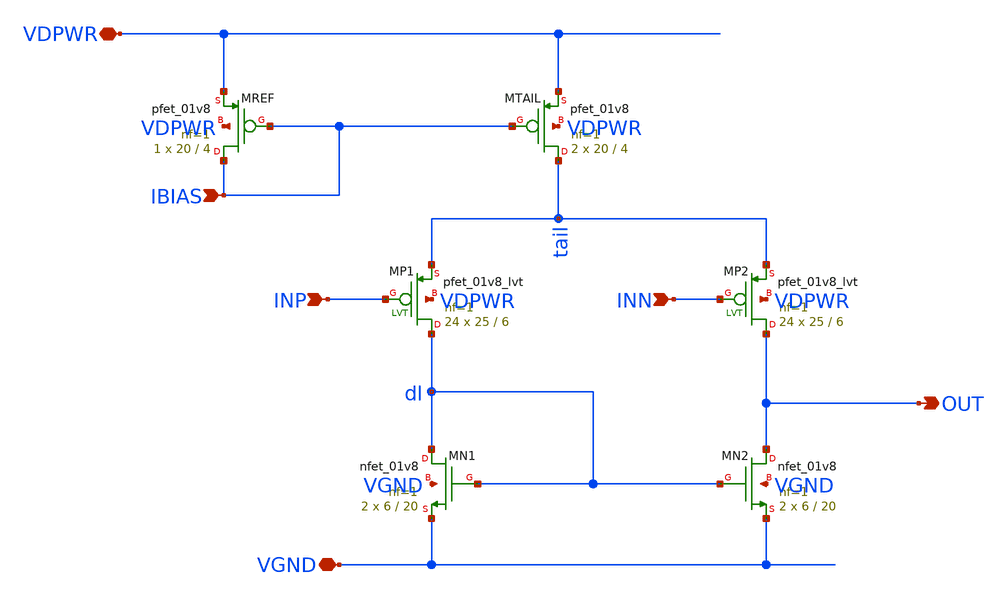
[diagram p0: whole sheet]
** sch_path: xschem/ota5t.sch
**.subckt ota5t INP INN IBIAS OUT VDPWR VGND
*.ipin INP
*.ipin INN
*.ipin IBIAS
*.opin OUT
*.iopin VDPWR
*.iopin VGND
XMREF IBIAS IBIAS VDPWR VDPWR sky130_fd_pr__pfet_01v8 L=4 W=20 nf=1 ad='int((1 + 1)/2) * 20 / 1 * 0.29'
+ as='int((1 + 2)/2) * 20 / 1 * 0.29' pd='2*int((1 + 1)/2) * (20 / 1 + 0.29)' ps='2*int((1 + 2)/2) * (20 / 1 + 0.29)'
+ nrd='0.29 / 20 ' nrs='0.29 / 20 ' sa=0 sb=0 sd=0 mult=1 m=1
XMTAIL tail IBIAS VDPWR VDPWR sky130_fd_pr__pfet_01v8 L=4 W=20 nf=1 ad='int((1 + 1)/2) * 20 / 1 * 0.29'
+ as='int((1 + 2)/2) * 20 / 1 * 0.29' pd='2*int((1 + 1)/2) * (20 / 1 + 0.29)' ps='2*int((1 + 2)/2) * (20 / 1 + 0.29)'
+ nrd='0.29 / 20 ' nrs='0.29 / 20 ' sa=0 sb=0 sd=0 mult=2 m=2
XMP1 dl INP tail VDPWR sky130_fd_pr__pfet_01v8_lvt L=6 W=25 nf=1 ad='int((1 + 1)/2) * 25 / 1 * 0.29'
+ as='int((1 + 2)/2) * 25 / 1 * 0.29' pd='2*int((1 + 1)/2) * (25 / 1 + 0.29)' ps='2*int((1 + 2)/2) * (25 / 1 + 0.29)'
+ nrd='0.29 / 25 ' nrs='0.29 / 25 ' sa=0 sb=0 sd=0 mult=24 m=24
XMP2 OUT INN tail VDPWR sky130_fd_pr__pfet_01v8_lvt L=6 W=25 nf=1 ad='int((1 + 1)/2) * 25 / 1 * 0.29'
+ as='int((1 + 2)/2) * 25 / 1 * 0.29' pd='2*int((1 + 1)/2) * (25 / 1 + 0.29)' ps='2*int((1 + 2)/2) * (25 / 1 + 0.29)'
+ nrd='0.29 / 25 ' nrs='0.29 / 25 ' sa=0 sb=0 sd=0 mult=24 m=24
XMN1 dl dl VGND VGND sky130_fd_pr__nfet_01v8 L=20 W=6 nf=1 ad='int((1 + 1)/2) * 6 / 1 * 0.29' as='int((1 + 2)/2) * 6 / 1 * 0.29'
+ pd='2*int((1 + 1)/2) * (6 / 1 + 0.29)' ps='2*int((1 + 2)/2) * (6 / 1 + 0.29)' nrd='0.29 / 6 ' nrs='0.29 / 6 '
+ sa=0 sb=0 sd=0 mult=2 m=2
XMN2 OUT dl VGND VGND sky130_fd_pr__nfet_01v8 L=20 W=6 nf=1 ad='int((1 + 1)/2) * 6 / 1 * 0.29' as='int((1 + 2)/2) * 6 / 1 * 0.29'
+ pd='2*int((1 + 1)/2) * (6 / 1 + 0.29)' ps='2*int((1 + 2)/2) * (6 / 1 + 0.29)' nrd='0.29 / 6 ' nrs='0.29 / 6 '
+ sa=0 sb=0 sd=0 mult=2 m=2
**.ends
.end
